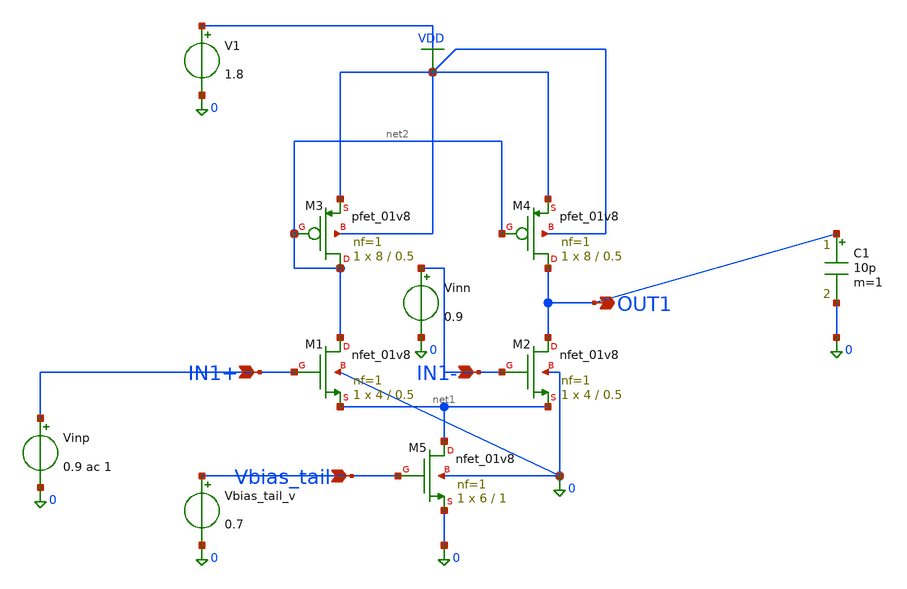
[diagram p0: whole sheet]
** sch_path: ota1_ac_ok.sch
**.subckt ota1_ac_ok IN1+ IN1- OUT1 Vbias_tail
*.ipin IN1+
*.ipin IN1-
*.opin OUT1
*.ipin Vbias_tail
XM1 net2 IN1+ net1 0 sky130_fd_pr__nfet_01v8 L=0.5 W=4 nf=1 ad='int((1 + 1)/2) * 4 / 1 * 0.29' as='int((1 + 2)/2) * 4 / 1 * 0.29'
+ pd='2*int((1 + 1)/2) * (4 / 1 + 0.29)' ps='2*int((1 + 2)/2) * (4 / 1 + 0.29)' nrd='0.29 / 4 ' nrs='0.29 / 4 '
+ sa=0 sb=0 sd=0 mult=1 m=1
XM2 OUT1 IN1- net1 0 sky130_fd_pr__nfet_01v8 L=0.5 W=4 nf=1 ad='int((1 + 1)/2) * 4 / 1 * 0.29' as='int((1 + 2)/2) * 4 / 1 * 0.29'
+ pd='2*int((1 + 1)/2) * (4 / 1 + 0.29)' ps='2*int((1 + 2)/2) * (4 / 1 + 0.29)' nrd='0.29 / 4 ' nrs='0.29 / 4 '
+ sa=0 sb=0 sd=0 mult=1 m=1
XM3 net2 net2 VDD VDD sky130_fd_pr__pfet_01v8 L=0.5 W=8 nf=1 ad='int((1 + 1)/2) * 8 / 1 * 0.29' as='int((1 + 2)/2) * 8 / 1 * 0.29'
+ pd='2*int((1 + 1)/2) * (8 / 1 + 0.29)' ps='2*int((1 + 2)/2) * (8 / 1 + 0.29)' nrd='0.29 / 8 ' nrs='0.29 / 8 '
+ sa=0 sb=0 sd=0 mult=1 m=1
XM4 OUT1 net2 VDD VDD sky130_fd_pr__pfet_01v8 L=0.5 W=8 nf=1 ad='int((1 + 1)/2) * 8 / 1 * 0.29' as='int((1 + 2)/2) * 8 / 1 * 0.29'
+ pd='2*int((1 + 1)/2) * (8 / 1 + 0.29)' ps='2*int((1 + 2)/2) * (8 / 1 + 0.29)' nrd='0.29 / 8 ' nrs='0.29 / 8 '
+ sa=0 sb=0 sd=0 mult=1 m=1
XM5 net1 Vbias_tail 0 0 sky130_fd_pr__nfet_01v8 L=1 W=6 nf=1 ad='int((1 + 1)/2) * 6 / 1 * 0.29' as='int((1 + 2)/2) * 6 / 1 * 0.29'
+ pd='2*int((1 + 1)/2) * (6 / 1 + 0.29)' ps='2*int((1 + 2)/2) * (6 / 1 + 0.29)' nrd='0.29 / 6 ' nrs='0.29 / 6 '
+ sa=0 sb=0 sd=0 mult=1 m=1
Vinp IN1+ 0 0.9 ac 1
V1 VDD 0 1.8
Vinn IN1- 0 0.9
Vbias_tail_v Vbias_tail 0 0.7
C1 OUT1 0 10p m=1
**** begin user architecture code

.lib /foss/pdks/sky130A/libs.tech/combined/sky130.lib.spice tt


.ac dec 20 1 1G

**** end user architecture code
**.ends
.GLOBAL VDD
.end
